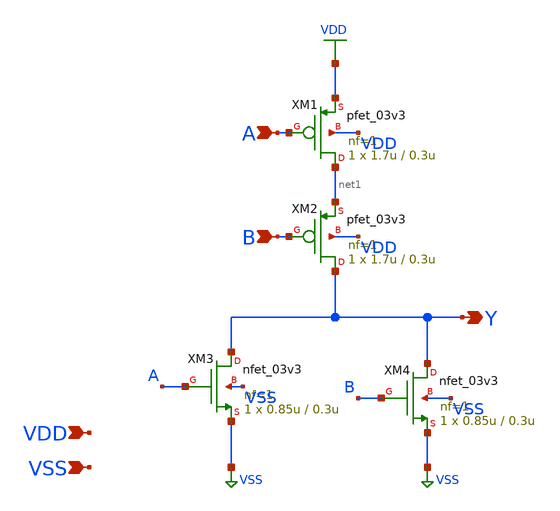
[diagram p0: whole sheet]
** sch_path: gf180mcu_osu_sc_gp9t3v3/xschem/gf180mcu_osu_sc_gp9t3v3__nor2_1.sch
**.subckt gf180mcu_osu_sc_gp9t3v3__nor2_1 A B Y VDD VSS
*.ipin A
*.ipin B
*.opin Y
*.ipin VDD
*.ipin VSS
XM1 net1 A VDD VDD pfet_03v3 L=0.3u W=1.7u nf=1 ad='int((nf+1)/2) * W/nf * 0.18u' as='int((nf+2)/2) * W/nf * 0.18u'
+ pd='2*int((nf+1)/2) * (W/nf + 0.18u)' ps='2*int((nf+2)/2) * (W/nf + 0.18u)' nrd='0.18u / W' nrs='0.18u / W'
+ sa=0 sb=0 sd=0 m=1
XM2 Y B net1 VDD pfet_03v3 L=0.3u W=1.7u nf=1 ad='int((nf+1)/2) * W/nf * 0.18u' as='int((nf+2)/2) * W/nf * 0.18u'
+ pd='2*int((nf+1)/2) * (W/nf + 0.18u)' ps='2*int((nf+2)/2) * (W/nf + 0.18u)' nrd='0.18u / W' nrs='0.18u / W'
+ sa=0 sb=0 sd=0 m=1
XM3 Y A VSS VSS nfet_03v3 L=0.3u W=0.85u nf=1 ad='int((nf+1)/2) * W/nf * 0.18u' as='int((nf+2)/2) * W/nf * 0.18u'
+ pd='2*int((nf+1)/2) * (W/nf + 0.18u)' ps='2*int((nf+2)/2) * (W/nf + 0.18u)' nrd='0.18u / W' nrs='0.18u / W'
+ sa=0 sb=0 sd=0 m=1
XM4 Y B VSS VSS nfet_03v3 L=0.3u W=0.85u nf=1 ad='int((nf+1)/2) * W/nf * 0.18u' as='int((nf+2)/2) * W/nf * 0.18u'
+ pd='2*int((nf+1)/2) * (W/nf + 0.18u)' ps='2*int((nf+2)/2) * (W/nf + 0.18u)' nrd='0.18u / W' nrs='0.18u / W'
+ sa=0 sb=0 sd=0 m=1
**.ends
.GLOBAL VDD
.GLOBAL VSS
.end
